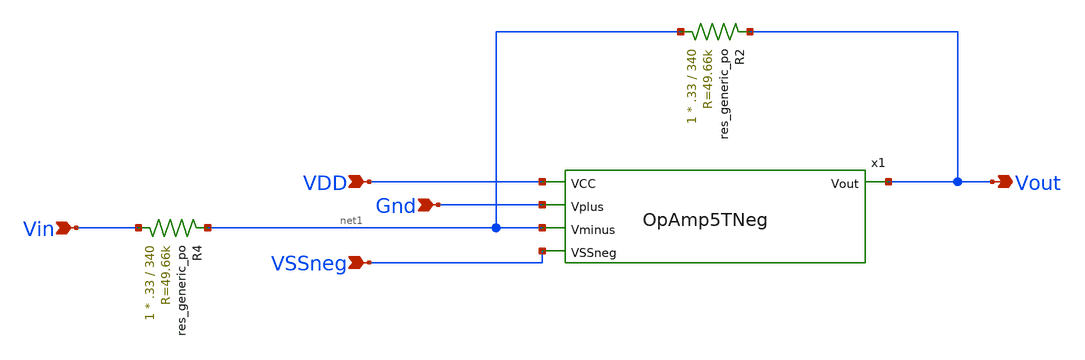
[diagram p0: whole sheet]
** sch_path: xschem/invOpAmp.sch
**.subckt invOpAmp Vout Vin VDD VSSneg Gnd
*.opin Vout
*.ipin Vin
*.ipin VDD
*.ipin VSSneg
*.ipin Gnd
XR2 net1 Vout sky130_fd_pr__res_generic_po W=.33 L=340 m=1
XR4 Vin net1 sky130_fd_pr__res_generic_po W=.33 L=340 m=1
x1 VDD Vout Gnd net1 VSSneg OpAmp5TNeg
**.ends

* expanding   symbol:  OpAmp5TNeg.sym # of pins=5
** sym_path: xschem/OpAmp5TNeg.sym
** sch_path: xschem/OpAmp5TNeg.sch
.subckt OpAmp5TNeg VCC Vout Vplus Vminus VSSneg
*.ipin VCC
*.ipin VSSneg
*.ipin Vplus
*.ipin Vminus
*.opin Vout
XM5 Vout net1 VCC VCC sky130_fd_pr__pfet_01v8_lvt L=2 W=8 nf=1 ad='W * 0.29' as='W * 0.29' pd='2*(W + 0.29)'
+ ps='2*(W + 0.29)' nrd=0 nrs=0 sa=0 sb=0 sd=0 mult=1 m=1
XM6 net1 net1 VCC VCC sky130_fd_pr__pfet_01v8_lvt L=2 W=8 nf=1 ad='W * 0.29' as='W * 0.29' pd='2*(W + 0.29)'
+ ps='2*(W + 0.29)' nrd=0 nrs=0 sa=0 sb=0 sd=0 mult=1 m=1
XM17 SN VCC VSSneg VSSneg sky130_fd_pr__nfet_01v8_lvt L=2 W=6 nf=1 ad='W * 0.29' as='W * 0.29' pd='2*(W + 0.29)'
+ ps='2*(W + 0.29)' nrd=0 nrs=0 sa=0 sb=0 sd=0 mult=1 m=1
XM23 Vout Vminus SN VSSneg sky130_fd_pr__nfet_01v8 L=2 W=4 nf=1 ad='W * 0.29' as='W * 0.29' pd='2*(W + 0.29)'
+ ps='2*(W + 0.29)' nrd=0 nrs=0 sa=0 sb=0 sd=0 mult=1 m=1
XM16 net1 Vplus SN VSSneg sky130_fd_pr__nfet_01v8 L=2 W=4 nf=1 ad='W * 0.29' as='W * 0.29' pd='2*(W + 0.29)'
+ ps='2*(W + 0.29)' nrd=0 nrs=0 sa=0 sb=0 sd=0 mult=1 m=1
.ends

.end
